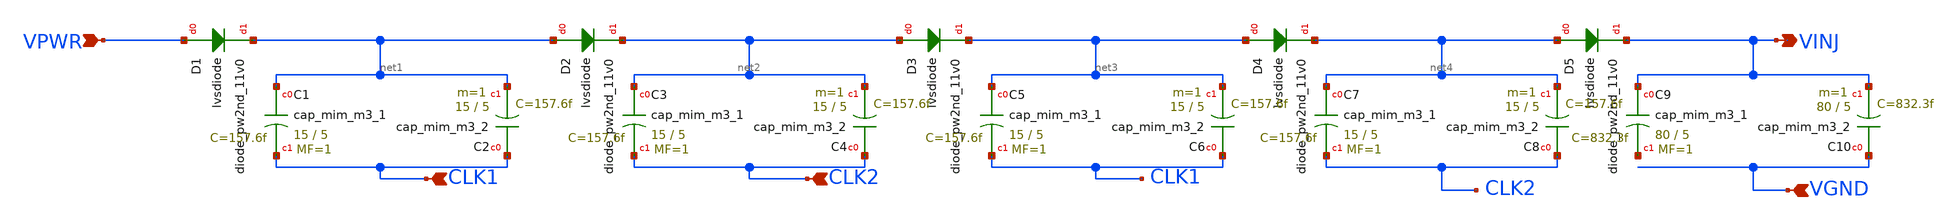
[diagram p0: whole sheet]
** sch_path: sky130_cells/ChargePump/dicksonpump.sch
**.subckt dicksonpump VINJ VPWR CLK1 CLK2 VGND
*.opin VINJ
*.ipin VPWR
*.ipin CLK1
*.ipin CLK2
*.ipin VGND
D1 VPWR net1 sky130_fd_pr__diode_pw2nd_11v0 area=50
D2 net1 net2 sky130_fd_pr__diode_pw2nd_11v0 area=50
D3 net2 net3 sky130_fd_pr__diode_pw2nd_11v0 area=50
D4 net3 net4 sky130_fd_pr__diode_pw2nd_11v0 area=50
D5 net4 VINJ sky130_fd_pr__diode_pw2nd_11v0 area=50
XC1 net1 CLK1 sky130_fd_pr__cap_mim_m3_1 W=15 L=5 MF=1 m=1
XC2 CLK1 net1 sky130_fd_pr__cap_mim_m3_2 W=15 L=5 MF=1 m=1
XC3 net2 CLK2 sky130_fd_pr__cap_mim_m3_1 W=15 L=5 MF=1 m=1
XC4 CLK2 net2 sky130_fd_pr__cap_mim_m3_2 W=15 L=5 MF=1 m=1
XC5 net3 CLK1 sky130_fd_pr__cap_mim_m3_1 W=15 L=5 MF=1 m=1
XC6 CLK1 net3 sky130_fd_pr__cap_mim_m3_2 W=15 L=5 MF=1 m=1
XC7 net4 CLK2 sky130_fd_pr__cap_mim_m3_1 W=15 L=5 MF=1 m=1
XC8 CLK2 net4 sky130_fd_pr__cap_mim_m3_2 W=15 L=5 MF=1 m=1
XC9 VINJ net5 sky130_fd_pr__cap_mim_m3_1 W=80 L=5 MF=1 m=1
XC10 VGND VINJ sky130_fd_pr__cap_mim_m3_2 W=80 L=5 MF=1 m=1
**.ends
.end
